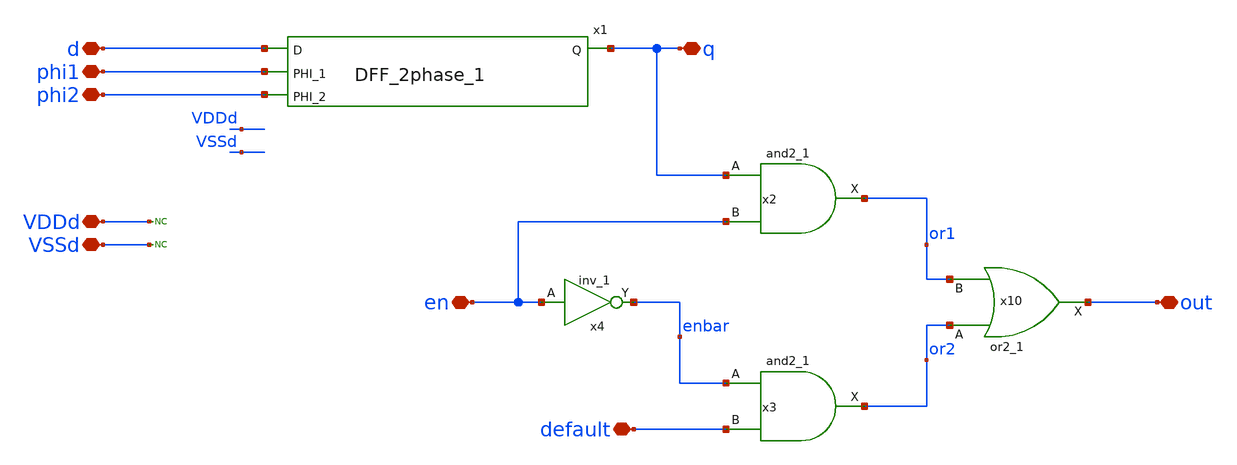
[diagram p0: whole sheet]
** sch_path: designs/libs/qw_core_analog/Register_unitcell/Register_unitcell.sch
**.subckt Register_unitcell phi1 phi2 d q en default out VDDd VSSd
*.iopin phi1
*.iopin phi2
*.iopin d
*.iopin q
*.iopin en
*.iopin default
*.iopin out
*.iopin VDDd
*.iopin VSSd
x4 en VSSd VDDd VSSd VDDd enbar gf180mcu_fd_sc_mcu9t5v0__inv_1
* noconn VDDd
* noconn VSSd
x1 d q phi1 phi2 DFF_2phase_1
x2 q en VSSd VDDd VSSd VDDd or1 gf180mcu_fd_sc_mcu9t5v0__and2_1
x10 or2 or1 VSSd VDDd VSSd VDDd out gf180mcu_fd_sc_mcu9t5v0__or2_1
x3 enbar default VSSd VDDd VSSd VDDd or2 gf180mcu_fd_sc_mcu9t5v0__and2_1
**.ends

* expanding   symbol:  libs/qw_core_analog/DFF_2phase_1/DFF_2phase_1.sym # of pins=4
** sym_path: designs/switch_matrix_gf180mcu_9t5v0-main/designs/libs/core_swmatrix/DFF_2phase_1.sym
** sch_path: designs/switch_matrix_gf180mcu_9t5v0-main/designs/libs/core_swmatrix/DFF_2phase_1.sch
.subckt DFF_2phase_1 D Q PHI_1 PHI_2
*.ipin D
*.ipin PHI_1
*.ipin PHI_2
*.opin Q
xmain D PHI_1 out_m VDDd VDDd VSSd VSSd gf180mcu_fd_sc_mcu9t5v0__latq_1
xsecondary out_m PHI_2 Q VDDd VDDd VSSd VSSd gf180mcu_fd_sc_mcu9t5v0__latq_1
.ends

.end
